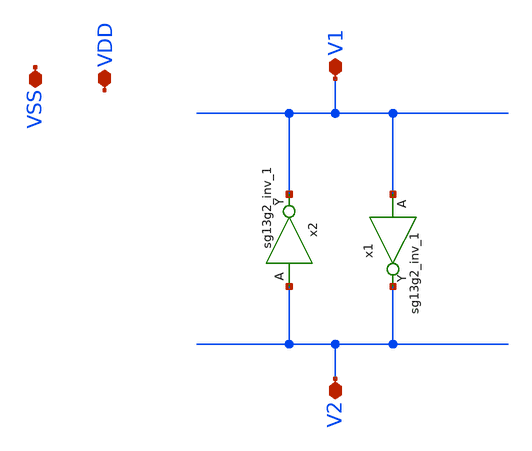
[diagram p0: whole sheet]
** sch_path: QDLL6501-main/schematic/xschem/LATCH.sch
**.subckt LATCH VDD VSS V1 V2
*.iopin VDD
*.iopin VSS
*.iopin V1
*.iopin V2
x1 V2 V1 VDD VSS sg13g2_inv_1
x2 V1 V2 VDD VSS sg13g2_inv_1
**.ends

* expanding   symbol:  sg13g2_stdcells/sg13g2_inv_1.sym # of pins=2
** sym_path: sg13g2_stdcells/sg13g2_inv_1.sym
** sch_path: sg13g2_stdcells/sg13g2_inv_1.sch
.subckt sg13g2_inv_1 Y A VDD VSS
*.opin Y
*.ipin A
*.iopin VDD
*.iopin VSS
XM1 Y A VSS VSS sg13_lv_nmos w=740.00n l=130.00n ng=1 m=1 mm_ok=1
XM2 Y A VDD VDD sg13_lv_pmos w=1.12u l=130.00n ng=1 m=1 mm_ok=1
.ends

.end
